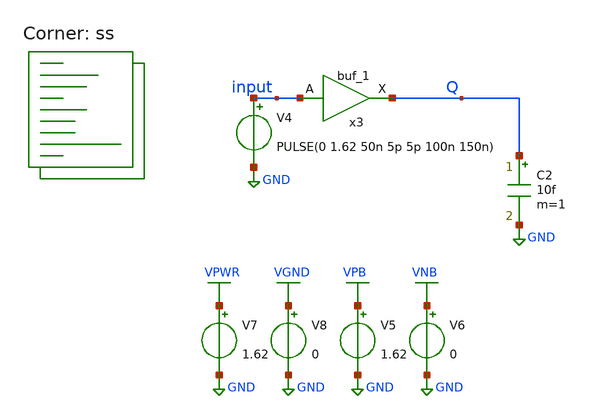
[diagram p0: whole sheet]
** sch_path: hgu/tb/tb_hgu_buff.sch
**.subckt tb_hgu_buff
V4 input GND PULSE(0 1.62 50n 5p 5p 100n 150n)
C2 Q GND 10f m=1
V5 VPB GND 1.62
V6 VNB GND 0
V7 VPWR GND 1.62
V8 VGND GND 0
x3 input VGND VNB VPB VPWR Q sky130_fd_sc_hd__buf_1
**** begin user architecture code


.save all
.temp = 100
.tran 100p 400n
.OPTIONS savecurrent
.include /foss/pdks/sky130A/libs.ref/sky130_fd_sc_hd/spice/sky130_fd_sc_hd.spice
.control
	run
        plot v(input) V(Q)
	let svdd = 1.62
	let max = svdd*0.8
	let min = svdd*0.2
	let mid = svdd*0.5
	meas tran rising_s find time when V(Q)=min RISE=1 TD=1000p
        meas tran rising_e find time when V(Q)=max RISE=1 TD=1000p
        let rising_time = rising_e-rising_s
        meas tran falling_s find time when V(Q)=max FALL=1 TD=1000p
        meas tran falling_e find time when V(Q)=min FALL=1 TD=1000p
        let falling_time = falling_e-falling_s
        meas tran IN find time when V(input)=mid RISE=1 TD=1000p
        meas tran OUT find time when V(Q)=mid RISE=1 TD=1000p
        let rising_delay = OUT-IN
	meas tran fIN find time when V(input)=mid FALL=1 TD=1000p
        meas tran fOUT find time when V(Q)=mid FALL=1 TD=1000p
        let falling_delay = fOUT-fIN

        print rising_time falling_time rising_delay falling_delay

.endc


.lib $::SKYWATER_MODELS/sky130.lib.spice ss
**** end user architecture code
**.ends
.GLOBAL GND
.GLOBAL VPB
.GLOBAL VNB
.GLOBAL VPWR
.GLOBAL VGND
.end
